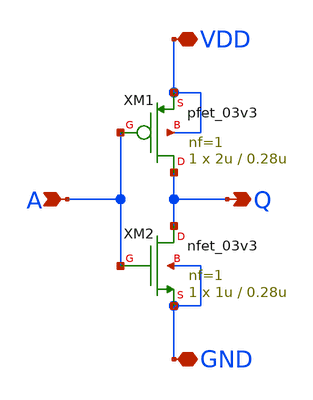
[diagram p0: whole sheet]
** sch_path: inv_test.sch
**.subckt inv_test Q A VDD GND
*.opin Q
*.ipin A
*.iopin VDD
*.iopin GND
XM1 Q A VDD VDD pfet_03v3 L=0.28u W=2u nf=1 ad='int((nf+1)/2) * W/nf * 0.18u' as='int((nf+2)/2) * W/nf * 0.18u'
+ pd='2*int((nf+1)/2) * (W/nf + 0.18u)' ps='2*int((nf+2)/2) * (W/nf + 0.18u)' nrd='0.18u / W' nrs='0.18u / W'
+ sa=0 sb=0 sd=0 m=1
XM2 Q A GND GND nfet_03v3 L=0.28u W=1u nf=1 ad='int((nf+1)/2) * W/nf * 0.18u' as='int((nf+2)/2) * W/nf * 0.18u'
+ pd='2*int((nf+1)/2) * (W/nf + 0.18u)' ps='2*int((nf+2)/2) * (W/nf + 0.18u)' nrd='0.18u / W' nrs='0.18u / W'
+ sa=0 sb=0 sd=0 m=1
**.ends
.end
